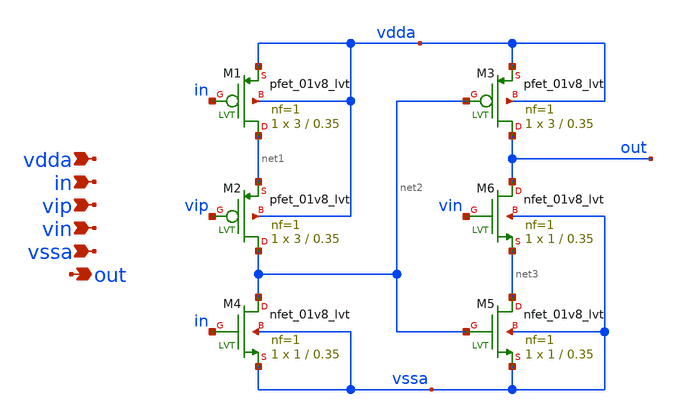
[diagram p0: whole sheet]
** sch_path: xschem/delay_cell_2.sch
**.subckt delay_cell_2 vdda in vip vin vssa out
*.ipin vdda
*.ipin in
*.ipin vip
*.ipin vin
*.ipin vssa
*.opin out
XM1 net1 in vdda vdda sky130_fd_pr__pfet_01v8_lvt L=0.35 W=3 nf=1 ad='int((nf+1)/2) * W/nf * 0.29' as='int((nf+2)/2) * W/nf * 0.29'
+ pd='2*int((nf+1)/2) * (W/nf + 0.29)' ps='2*int((nf+2)/2) * (W/nf + 0.29)' nrd='0.29 / W' nrs='0.29 / W'
+ sa=0 sb=0 sd=0 mult=1 m=1
XM2 net2 vip net1 vdda sky130_fd_pr__pfet_01v8_lvt L=0.35 W=3 nf=1 ad='int((nf+1)/2) * W/nf * 0.29' as='int((nf+2)/2) * W/nf * 0.29'
+ pd='2*int((nf+1)/2) * (W/nf + 0.29)' ps='2*int((nf+2)/2) * (W/nf + 0.29)' nrd='0.29 / W' nrs='0.29 / W'
+ sa=0 sb=0 sd=0 mult=1 m=1
XM3 out net2 vdda vdda sky130_fd_pr__pfet_01v8_lvt L=0.35 W=3 nf=1 ad='int((nf+1)/2) * W/nf * 0.29' as='int((nf+2)/2) * W/nf * 0.29'
+ pd='2*int((nf+1)/2) * (W/nf + 0.29)' ps='2*int((nf+2)/2) * (W/nf + 0.29)' nrd='0.29 / W' nrs='0.29 / W'
+ sa=0 sb=0 sd=0 mult=1 m=1
XM4 net2 in vssa vssa sky130_fd_pr__nfet_01v8_lvt L=0.35 W=1 nf=1 ad='int((nf+1)/2) * W/nf * 0.29' as='int((nf+2)/2) * W/nf * 0.29'
+ pd='2*int((nf+1)/2) * (W/nf + 0.29)' ps='2*int((nf+2)/2) * (W/nf + 0.29)' nrd='0.29 / W' nrs='0.29 / W'
+ sa=0 sb=0 sd=0 mult=1 m=1
XM5 net3 net2 vssa vssa sky130_fd_pr__nfet_01v8_lvt L=0.35 W=1 nf=1 ad='int((nf+1)/2) * W/nf * 0.29'
+ as='int((nf+2)/2) * W/nf * 0.29' pd='2*int((nf+1)/2) * (W/nf + 0.29)' ps='2*int((nf+2)/2) * (W/nf + 0.29)'
+ nrd='0.29 / W' nrs='0.29 / W' sa=0 sb=0 sd=0 mult=1 m=1
XM6 out vin net3 vssa sky130_fd_pr__nfet_01v8_lvt L=0.35 W=1 nf=1 ad='int((nf+1)/2) * W/nf * 0.29' as='int((nf+2)/2) * W/nf * 0.29'
+ pd='2*int((nf+1)/2) * (W/nf + 0.29)' ps='2*int((nf+2)/2) * (W/nf + 0.29)' nrd='0.29 / W' nrs='0.29 / W'
+ sa=0 sb=0 sd=0 mult=1 m=1
**.ends
.end
